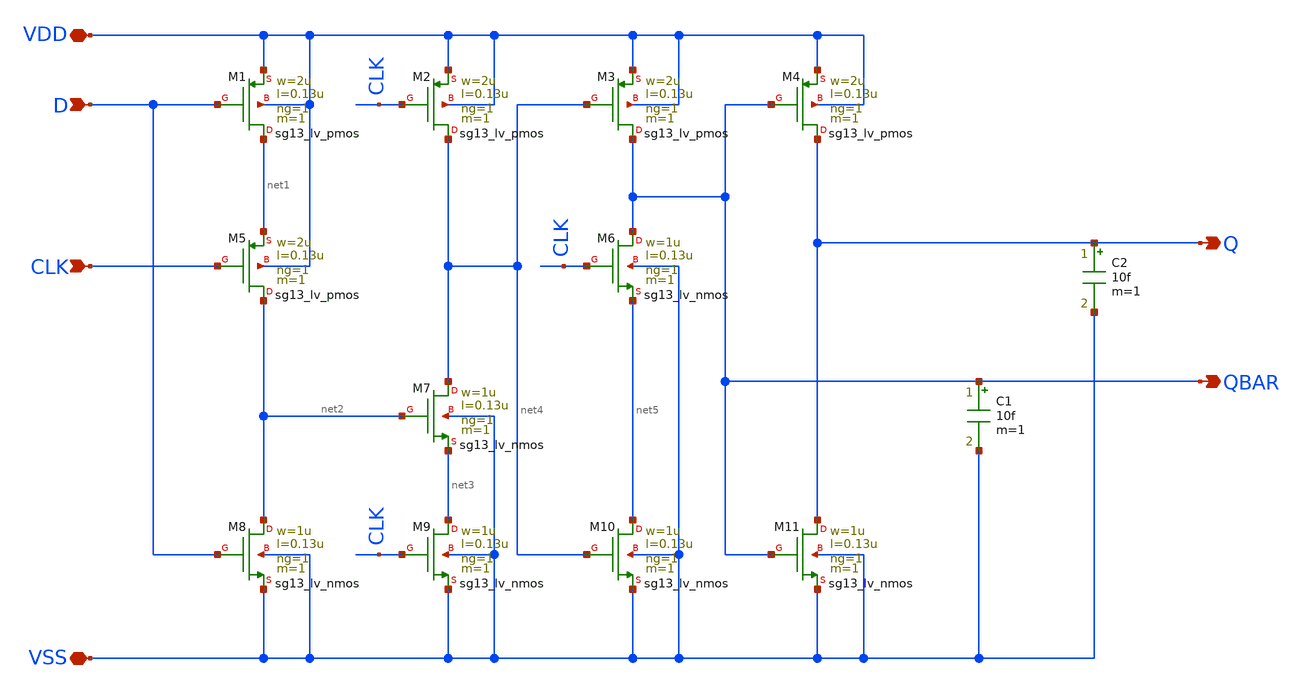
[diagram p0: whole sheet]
** sch_path: Team 1 Design/design_data/xschem/DFlop/DFlop.sch
**.subckt DFlop VDD VSS D CLK Q QBAR
*.iopin VDD
*.iopin VSS
*.ipin D
*.ipin CLK
*.opin Q
*.opin QBAR
XM1 net1 D VDD VDD sg13_lv_pmos w=2u l=0.13u ng=1 m=1 mm_ok=1
XM2 net4 CLK VDD VDD sg13_lv_pmos w=2u l=0.13u ng=1 m=1 mm_ok=1
XM3 QBAR net4 VDD VDD sg13_lv_pmos w=2u l=0.13u ng=1 m=1 mm_ok=1
XM4 Q QBAR VDD VDD sg13_lv_pmos w=2u l=0.13u ng=1 m=1 mm_ok=1
XM5 net2 CLK net1 VDD sg13_lv_pmos w=2u l=0.13u ng=1 m=1 mm_ok=1
XM6 QBAR CLK net5 VSS sg13_lv_nmos w=1u l=0.13u ng=1 m=1 mm_ok=1
XM7 net4 net2 net3 VSS sg13_lv_nmos w=1u l=0.13u ng=1 m=1 mm_ok=1
XM8 net2 D VSS VSS sg13_lv_nmos w=1u l=0.13u ng=1 m=1 mm_ok=1
XM9 net3 CLK VSS VSS sg13_lv_nmos w=1u l=0.13u ng=1 m=1 mm_ok=1
XM10 net5 net4 VSS VSS sg13_lv_nmos w=1u l=0.13u ng=1 m=1 mm_ok=1
XM11 Q QBAR VSS VSS sg13_lv_nmos w=1u l=0.13u ng=1 m=1 mm_ok=1
C1 QBAR VSS 10f m=1
C2 Q VSS 10f m=1
**.ends
.end
